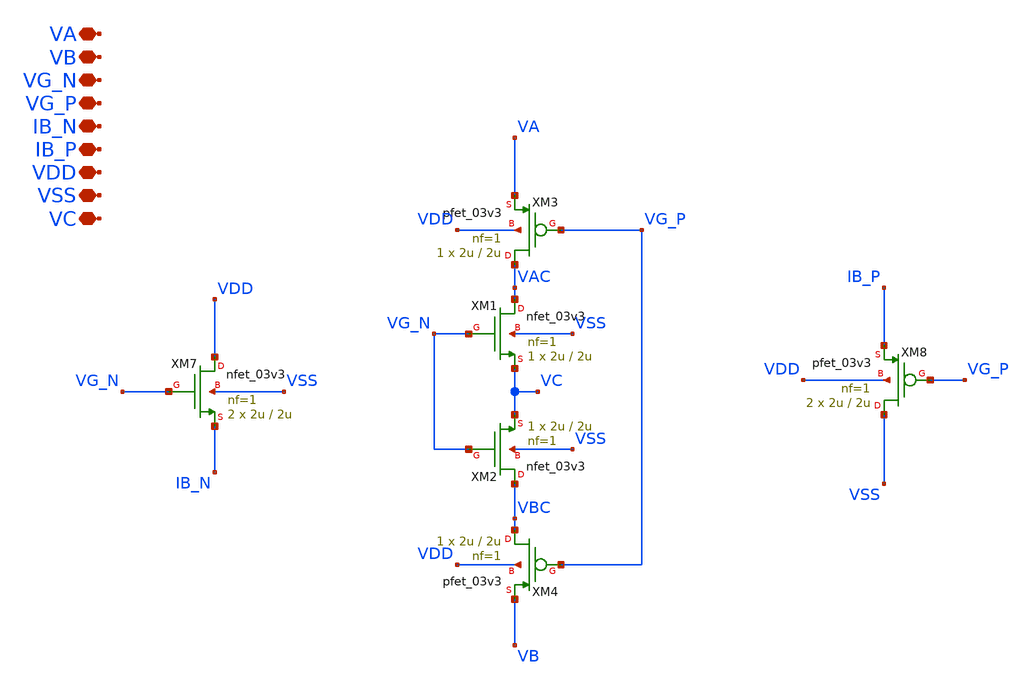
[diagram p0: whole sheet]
** sch_path: TIA/xschem/PseudoResistor/PR_single.sch
**.subckt PR_single VA VB VG_N VG_P IB_N IB_P VDD VSS VC
*.iopin VA
*.iopin VB
*.iopin VG_N
*.iopin VG_P
*.iopin IB_N
*.iopin IB_P
*.iopin VDD
*.iopin VSS
*.iopin VC
XM1 VAC VG_N VC VSS nfet_03v3 L=2u W=2u nf=1 ad='int((nf+1)/2) * W/nf * 0.18u' as='int((nf+2)/2) * W/nf * 0.18u'
+ pd='2*int((nf+1)/2) * (W/nf + 0.18u)' ps='2*int((nf+2)/2) * (W/nf + 0.18u)' nrd='0.18u / W' nrs='0.18u / W'
+ sa=0 sb=0 sd=0 m=1
XM3 VAC VG_P VA VDD pfet_03v3 L=2u W=2u nf=1 ad='int((nf+1)/2) * W/nf * 0.18u' as='int((nf+2)/2) * W/nf * 0.18u'
+ pd='2*int((nf+1)/2) * (W/nf + 0.18u)' ps='2*int((nf+2)/2) * (W/nf + 0.18u)' nrd='0.18u / W' nrs='0.18u / W'
+ sa=0 sb=0 sd=0 m=1
XM2 VBC VG_N VC VSS nfet_03v3 L=2u W=2u nf=1 ad='int((nf+1)/2) * W/nf * 0.18u' as='int((nf+2)/2) * W/nf * 0.18u'
+ pd='2*int((nf+1)/2) * (W/nf + 0.18u)' ps='2*int((nf+2)/2) * (W/nf + 0.18u)' nrd='0.18u / W' nrs='0.18u / W'
+ sa=0 sb=0 sd=0 m=1
XM4 VBC VG_P VB VDD pfet_03v3 L=2u W=2u nf=1 ad='int((nf+1)/2) * W/nf * 0.18u' as='int((nf+2)/2) * W/nf * 0.18u'
+ pd='2*int((nf+1)/2) * (W/nf + 0.18u)' ps='2*int((nf+2)/2) * (W/nf + 0.18u)' nrd='0.18u / W' nrs='0.18u / W'
+ sa=0 sb=0 sd=0 m=1
XM7 VDD VG_N IB_N VSS nfet_03v3 L=2u W=2u nf=1 ad='int((nf+1)/2) * W/nf * 0.18u' as='int((nf+2)/2) * W/nf * 0.18u'
+ pd='2*int((nf+1)/2) * (W/nf + 0.18u)' ps='2*int((nf+2)/2) * (W/nf + 0.18u)' nrd='0.18u / W' nrs='0.18u / W'
+ sa=0 sb=0 sd=0 m=2
XM8 VSS VG_P IB_P VDD pfet_03v3 L=2u W=2u nf=1 ad='int((nf+1)/2) * W/nf * 0.18u' as='int((nf+2)/2) * W/nf * 0.18u'
+ pd='2*int((nf+1)/2) * (W/nf + 0.18u)' ps='2*int((nf+2)/2) * (W/nf + 0.18u)' nrd='0.18u / W' nrs='0.18u / W'
+ sa=0 sb=0 sd=0 m=2
**.ends
.end
